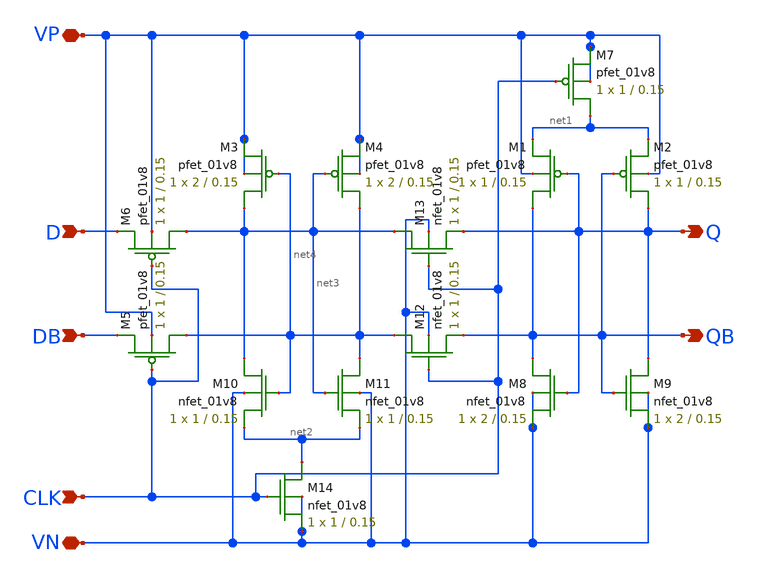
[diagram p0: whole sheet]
** sch_path: MP2/xschem/archive/csrl_dff.sch
**.subckt csrl_dff D DB VP VN CLK QB Q
*.ipin D
*.ipin DB
*.iopin VP
*.iopin VN
*.ipin CLK
*.opin QB
*.opin Q
XM1 QB Q net1 VP sky130_fd_pr__pfet_01v8 L=0.15 W=1 nf=1 ad='int((nf+1)/2) * W/nf * 0.29' as='int((nf+2)/2) * W/nf * 0.29'
+ pd='2*int((nf+1)/2) * (W/nf + 0.29)' ps='2*int((nf+2)/2) * (W/nf + 0.29)' nrd='0.29 / W' nrs='0.29 / W'
+ sa=0 sb=0 sd=0 mult=1 m=1
XM2 Q QB net1 VP sky130_fd_pr__pfet_01v8 L=0.15 W=1 nf=1 ad='int((nf+1)/2) * W/nf * 0.29' as='int((nf+2)/2) * W/nf * 0.29'
+ pd='2*int((nf+1)/2) * (W/nf + 0.29)' ps='2*int((nf+2)/2) * (W/nf + 0.29)' nrd='0.29 / W' nrs='0.29 / W'
+ sa=0 sb=0 sd=0 mult=1 m=1
XM3 net3 net4 VP VP sky130_fd_pr__pfet_01v8 L=0.15 W=2 nf=1 ad='int((nf+1)/2) * W/nf * 0.29' as='int((nf+2)/2) * W/nf * 0.29'
+ pd='2*int((nf+1)/2) * (W/nf + 0.29)' ps='2*int((nf+2)/2) * (W/nf + 0.29)' nrd='0.29 / W' nrs='0.29 / W'
+ sa=0 sb=0 sd=0 mult=1 m=1
XM4 net4 net3 VP VP sky130_fd_pr__pfet_01v8 L=0.15 W=2 nf=1 ad='int((nf+1)/2) * W/nf * 0.29' as='int((nf+2)/2) * W/nf * 0.29'
+ pd='2*int((nf+1)/2) * (W/nf + 0.29)' ps='2*int((nf+2)/2) * (W/nf + 0.29)' nrd='0.29 / W' nrs='0.29 / W'
+ sa=0 sb=0 sd=0 mult=1 m=1
XM8 QB Q VN VN sky130_fd_pr__nfet_01v8 L=0.15 W=2 nf=1 ad='int((nf+1)/2) * W/nf * 0.29' as='int((nf+2)/2) * W/nf * 0.29'
+ pd='2*int((nf+1)/2) * (W/nf + 0.29)' ps='2*int((nf+2)/2) * (W/nf + 0.29)' nrd='0.29 / W' nrs='0.29 / W'
+ sa=0 sb=0 sd=0 mult=1 m=1
XM7 net1 CLK VP VP sky130_fd_pr__pfet_01v8 L=0.15 W=1 nf=1 ad='int((nf+1)/2) * W/nf * 0.29' as='int((nf+2)/2) * W/nf * 0.29'
+ pd='2*int((nf+1)/2) * (W/nf + 0.29)' ps='2*int((nf+2)/2) * (W/nf + 0.29)' nrd='0.29 / W' nrs='0.29 / W'
+ sa=0 sb=0 sd=0 mult=1 m=1
XM9 Q QB VN VN sky130_fd_pr__nfet_01v8 L=0.15 W=2 nf=1 ad='int((nf+1)/2) * W/nf * 0.29' as='int((nf+2)/2) * W/nf * 0.29'
+ pd='2*int((nf+1)/2) * (W/nf + 0.29)' ps='2*int((nf+2)/2) * (W/nf + 0.29)' nrd='0.29 / W' nrs='0.29 / W'
+ sa=0 sb=0 sd=0 mult=1 m=1
XM10 net3 net4 net2 VN sky130_fd_pr__nfet_01v8 L=0.15 W=1 nf=1 ad='int((nf+1)/2) * W/nf * 0.29' as='int((nf+2)/2) * W/nf * 0.29'
+ pd='2*int((nf+1)/2) * (W/nf + 0.29)' ps='2*int((nf+2)/2) * (W/nf + 0.29)' nrd='0.29 / W' nrs='0.29 / W'
+ sa=0 sb=0 sd=0 mult=1 m=1
XM11 net4 net3 net2 VN sky130_fd_pr__nfet_01v8 L=0.15 W=1 nf=1 ad='int((nf+1)/2) * W/nf * 0.29' as='int((nf+2)/2) * W/nf * 0.29'
+ pd='2*int((nf+1)/2) * (W/nf + 0.29)' ps='2*int((nf+2)/2) * (W/nf + 0.29)' nrd='0.29 / W' nrs='0.29 / W'
+ sa=0 sb=0 sd=0 mult=1 m=1
XM12 net4 CLK QB VN sky130_fd_pr__nfet_01v8 L=0.15 W=1 nf=1 ad='int((nf+1)/2) * W/nf * 0.29' as='int((nf+2)/2) * W/nf * 0.29'
+ pd='2*int((nf+1)/2) * (W/nf + 0.29)' ps='2*int((nf+2)/2) * (W/nf + 0.29)' nrd='0.29 / W' nrs='0.29 / W'
+ sa=0 sb=0 sd=0 mult=1 m=1
XM13 net3 CLK Q VN sky130_fd_pr__nfet_01v8 L=0.15 W=1 nf=1 ad='int((nf+1)/2) * W/nf * 0.29' as='int((nf+2)/2) * W/nf * 0.29'
+ pd='2*int((nf+1)/2) * (W/nf + 0.29)' ps='2*int((nf+2)/2) * (W/nf + 0.29)' nrd='0.29 / W' nrs='0.29 / W'
+ sa=0 sb=0 sd=0 mult=1 m=1
XM14 net2 CLK VN VN sky130_fd_pr__nfet_01v8 L=0.15 W=1 nf=1 ad='int((nf+1)/2) * W/nf * 0.29' as='int((nf+2)/2) * W/nf * 0.29'
+ pd='2*int((nf+1)/2) * (W/nf + 0.29)' ps='2*int((nf+2)/2) * (W/nf + 0.29)' nrd='0.29 / W' nrs='0.29 / W'
+ sa=0 sb=0 sd=0 mult=1 m=1
XM5 net4 CLK DB VP sky130_fd_pr__pfet_01v8 L=0.15 W=1 nf=1 ad='int((nf+1)/2) * W/nf * 0.29' as='int((nf+2)/2) * W/nf * 0.29'
+ pd='2*int((nf+1)/2) * (W/nf + 0.29)' ps='2*int((nf+2)/2) * (W/nf + 0.29)' nrd='0.29 / W' nrs='0.29 / W'
+ sa=0 sb=0 sd=0 mult=1 m=1
XM6 net3 CLK D VP sky130_fd_pr__pfet_01v8 L=0.15 W=1 nf=1 ad='int((nf+1)/2) * W/nf * 0.29' as='int((nf+2)/2) * W/nf * 0.29'
+ pd='2*int((nf+1)/2) * (W/nf + 0.29)' ps='2*int((nf+2)/2) * (W/nf + 0.29)' nrd='0.29 / W' nrs='0.29 / W'
+ sa=0 sb=0 sd=0 mult=1 m=1
**.ends
.end
